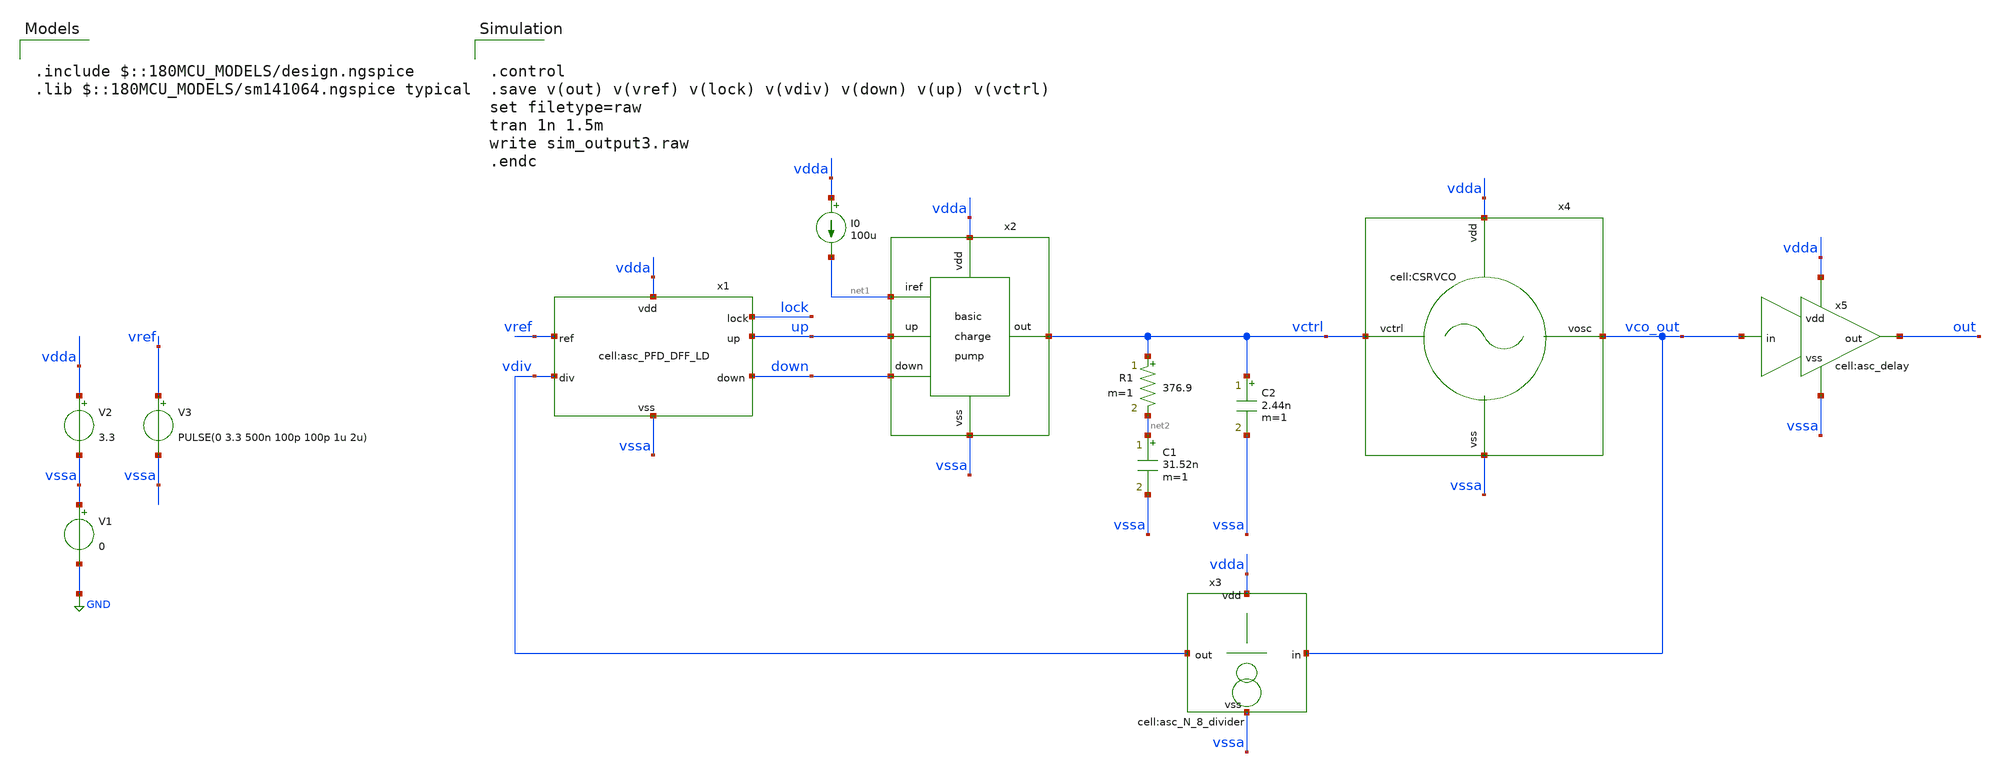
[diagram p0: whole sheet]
** sch_path: designs/libs/tb_analog/tb_asc_lock_detector/tb_asc_lock_detector.sch
**.subckt tb_asc_lock_detector
V1 vssa GND 0
V2 vdda vssa 3.3
V3 vref vssa PULSE(0 3.3 500n 100p 100p 1u 2u)
x2 vdda vctrl vssa down up net1 asc_basic_pump
I0 vdda net1 100u
x3 vco_out vdiv vdda vssa asc_N_8_divider
x4 vctrl vdda vssa vco_out CSRVCO
x5 vco_out vssa out vdda asc_delay
C1 net2 vssa 31.52n m=1
C2 vctrl vssa 2.44n m=1
R1 vctrl net2 376.9 m=1
x1 vdda lock vssa vdiv vref up down asc_PFD_DFF_LD
**** begin user architecture code

.include $::180MCU_MODELS/design.ngspice
.lib $::180MCU_MODELS/sm141064.ngspice typical



.control
.save v(out) v(vref) v(lock) v(vdiv) v(down) v(up) v(vctrl)
set filetype=raw
tran 1n 1.5m
write sim_output3.raw
.endc


**** end user architecture code
**.ends
.GLOBAL GND
.end
